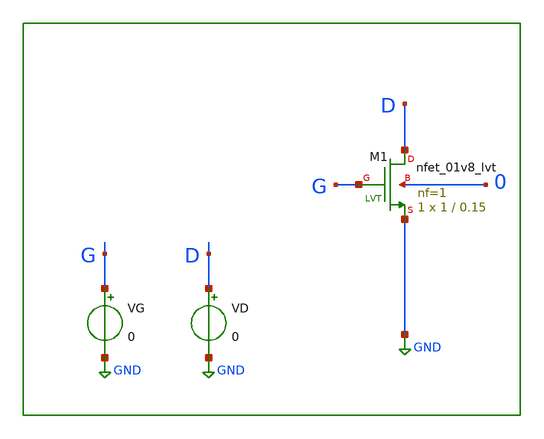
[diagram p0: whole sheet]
** sch_path: circuit_model/tb/NMOS.sch
**.subckt NMOS
VG G GND 0
VD D GND 0
XM1 D G GND 0 sky130_fd_pr__nfet_01v8_lvt L=0.15 W=1 nf=1 ad='int((nf+1)/2) * W/nf * 0.29' as='int((nf+2)/2) * W/nf * 0.29'
+ pd='2*int((nf+1)/2) * (W/nf + 0.29)' ps='2*int((nf+2)/2) * (W/nf + 0.29)' nrd='0.29 / W' nrs='0.29 / W'
+ sa=0 sb=0 sd=0 mult=1 m=1
**** begin user architecture code


.lib /home/dkits/efabless/mpw-5/pdks/sky130A/libs.tech/ngspice/sky130.lib.spice tt
.inc /home/dkits/efabless/mpw-5/pdks/sky130A/libs.ref/sky130_fd_sc_hd/spice/sky130_fd_sc_hd.spice




.control
set nobreak
set numthread=11

dc VD 0 2 0.01 VG 0 2 0.2
print format=raw file=NMOS.raw v(*) i(*)

.endc


**** end user architecture code
**.ends
.GLOBAL GND
.end
